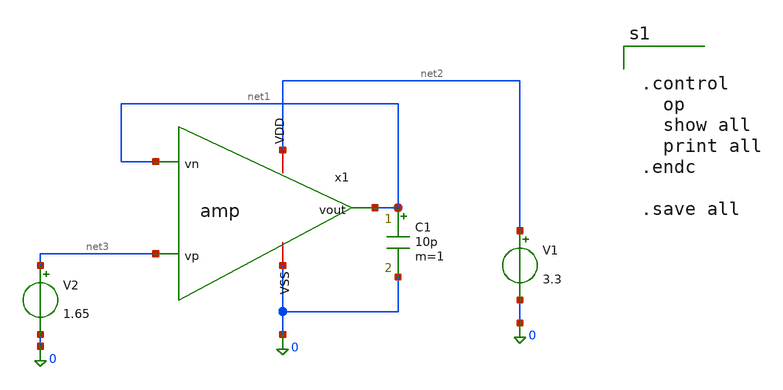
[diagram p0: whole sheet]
** sch_path: xschem/amp_tb.sch
**.subckt amp_tb
x1 net2 net1 net1 net3 0 amp
V1 net2 0 3.3
V2 net3 0 1.65
C1 net1 0 10p m=1
**** begin user architecture code


.control
  op
  show all
  print all
.endc

.save all




.param fnoicor=0
.param sw_stat_global=0
.param sw_stat_mismatch=0
.param mc_skew=0
.param res_mc_skew=0
.param cap_mc_skew=0

.lib /foss/pdks/ciel/gf180mcu/versions/026824c7969ce6f4fc9678e6ca04b0a06a596c4b/gf180mcuD/libs.tech/ngspice/sm141064.ngspice typical
.lib /foss/pdks/ciel/gf180mcu/versions/026824c7969ce6f4fc9678e6ca04b0a06a596c4b/gf180mcuD/libs.tech/ngspice/sm141064.ngspice res_typical


**** end user architecture code
**.ends

* expanding   symbol:  xschem/amp.sym # of pins=5
** sym_path: xschem/amp.sym
** sch_path: xschem/amp.sch
.subckt amp VDD vout vn vp VSS
*.iopin VDD
*.iopin VSS
*.ipin vn
*.ipin vp
*.opin vout
XM1 net1 net1 VDD VDD pfet_03v3 L=0.5u W=8u nf=1 ad='int((nf+1)/2) * W/nf * 0.18u' as='int((nf+2)/2) * W/nf * 0.18u'
+ pd='2*int((nf+1)/2) * (W/nf + 0.18u)' ps='2*int((nf+2)/2) * (W/nf + 0.18u)' nrd='0.18u / W' nrs='0.18u / W'
+ sa=0 sb=0 sd=0 m=1 par=1
XM2 net3 net1 VDD VDD pfet_03v3 L=0.5u W=8u nf=1 ad='int((nf+1)/2) * W/nf * 0.18u' as='int((nf+2)/2) * W/nf * 0.18u'
+ pd='2*int((nf+1)/2) * (W/nf + 0.18u)' ps='2*int((nf+2)/2) * (W/nf + 0.18u)' nrd='0.18u / W' nrs='0.18u / W'
+ sa=0 sb=0 sd=0 m=1 par=1
XM3 net4 vp net3 VDD pfet_03v3 L=0.5u W=4u nf=1 ad='int((nf+1)/2) * W/nf * 0.18u' as='int((nf+2)/2) * W/nf * 0.18u'
+ pd='2*int((nf+1)/2) * (W/nf + 0.18u)' ps='2*int((nf+2)/2) * (W/nf + 0.18u)' nrd='0.18u / W' nrs='0.18u / W'
+ sa=0 sb=0 sd=0 m=1 par=1
XM4 net2 vn net3 VDD pfet_03v3 L=0.5u W=4u nf=1 ad='int((nf+1)/2) * W/nf * 0.18u' as='int((nf+2)/2) * W/nf * 0.18u'
+ pd='2*int((nf+1)/2) * (W/nf + 0.18u)' ps='2*int((nf+2)/2) * (W/nf + 0.18u)' nrd='0.18u / W' nrs='0.18u / W'
+ sa=0 sb=0 sd=0 m=1 par=1
XM5 vout net1 VDD VDD pfet_03v3 L=0.5u W=20u nf=1 ad='int((nf+1)/2) * W/nf * 0.18u' as='int((nf+2)/2) * W/nf * 0.18u'
+ pd='2*int((nf+1)/2) * (W/nf + 0.18u)' ps='2*int((nf+2)/2) * (W/nf + 0.18u)' nrd='0.18u / W' nrs='0.18u / W'
+ sa=0 sb=0 sd=0 m=1 par=1
XM6 net4 net2 VSS VSS nfet_03v3 L=0.5u W=1u nf=1 ad='int((nf+1)/2) * W/nf * 0.18u' as='int((nf+2)/2) * W/nf * 0.18u'
+ pd='2*int((nf+1)/2) * (W/nf + 0.18u)' ps='2*int((nf+2)/2) * (W/nf + 0.18u)' nrd='0.18u / W' nrs='0.18u / W'
+ sa=0 sb=0 sd=0 m=1 par=1
XM8 vout net4 VSS VSS nfet_03v3 L=0.5u W=5u nf=1 ad='int((nf+1)/2) * W/nf * 0.18u' as='int((nf+2)/2) * W/nf * 0.18u'
+ pd='2*int((nf+1)/2) * (W/nf + 0.18u)' ps='2*int((nf+2)/2) * (W/nf + 0.18u)' nrd='0.18u / W' nrs='0.18u / W'
+ sa=0 sb=0 sd=0 m=1 par=1
XR1 VSS net1 VSS ppolyf_u_1k r_width=1u r_length=120u m=1
C1 vout net4 2.5p m=1
XM7 net2 net2 VSS VSS nfet_03v3 L=0.5u W=1u nf=1 ad='int((nf+1)/2) * W/nf * 0.18u' as='int((nf+2)/2) * W/nf * 0.18u'
+ pd='2*int((nf+1)/2) * (W/nf + 0.18u)' ps='2*int((nf+2)/2) * (W/nf + 0.18u)' nrd='0.18u / W' nrs='0.18u / W'
+ sa=0 sb=0 sd=0 m=1 par=1
.ends

.end
